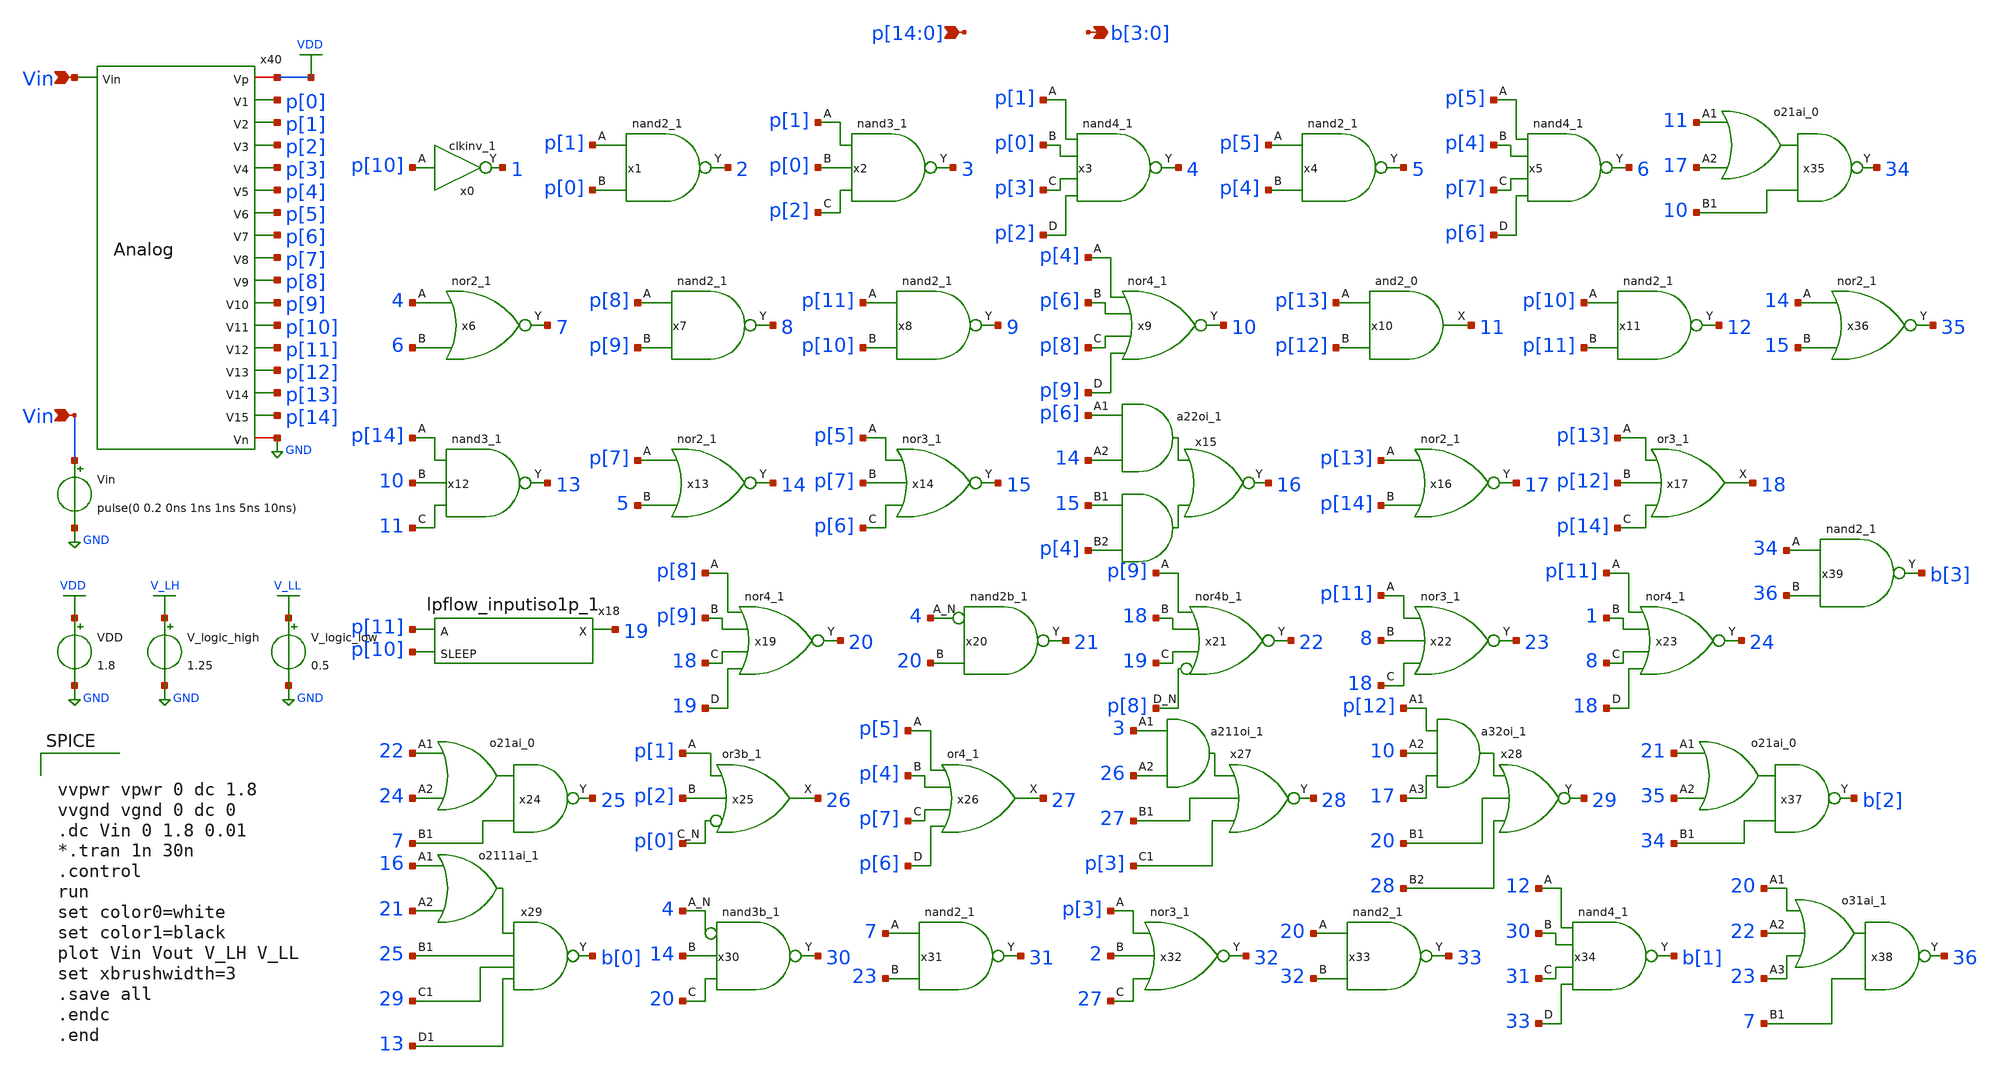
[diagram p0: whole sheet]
** sch_path: xschem/Vth_sch/Pre_layout/analog_therm.sch
**.subckt analog_therm
*+ p[14],p[13],p[12],p[11],p[10],p[9],p[8],p[7],p[6],p[5],p[4],p[3],p[2],p[1],p[0] b[3],b[2],b[1],b[0] Vin Vin
*.ipin p[14],p[13],p[12],p[11],p[10],p[9],p[8],p[7],p[6],p[5],p[4],p[3],p[2],p[1],p[0]
*.opin b[3],b[2],b[1],b[0]
*.ipin Vin
*.ipin Vin
x0 p[10] VGND VNB VPB VPWR 1 sky130_fd_sc_hd__clkinv_1
x1 p[1] p[0] VGND VNB VPB VPWR 2 sky130_fd_sc_hd__nand2_1
x2 p[1] p[0] p[2] VGND VNB VPB VPWR 3 sky130_fd_sc_hd__nand3_1
x3 p[1] p[0] p[3] p[2] VGND VNB VPB VPWR 4 sky130_fd_sc_hd__nand4_1
x4 p[5] p[4] VGND VNB VPB VPWR 5 sky130_fd_sc_hd__nand2_1
x5 p[5] p[4] p[7] p[6] VGND VNB VPB VPWR 6 sky130_fd_sc_hd__nand4_1
x6 4 6 VGND VNB VPB VPWR 7 sky130_fd_sc_hd__nor2_1
x7 p[8] p[9] VGND VNB VPB VPWR 8 sky130_fd_sc_hd__nand2_1
x8 p[11] p[10] VGND VNB VPB VPWR 9 sky130_fd_sc_hd__nand2_1
x9 p[4] p[6] p[8] p[9] VGND VNB VPB VPWR 10 sky130_fd_sc_hd__nor4_1
x10 p[13] p[12] VGND VNB VPB VPWR 11 sky130_fd_sc_hd__and2_0
x11 p[10] p[11] VGND VNB VPB VPWR 12 sky130_fd_sc_hd__nand2_1
x12 p[14] 10 11 VGND VNB VPB VPWR 13 sky130_fd_sc_hd__nand3_1
x13 p[7] 5 VGND VNB VPB VPWR 14 sky130_fd_sc_hd__nor2_1
x14 p[5] p[7] p[6] VGND VNB VPB VPWR 15 sky130_fd_sc_hd__nor3_1
x15 p[6] 14 15 p[4] VGND VNB VPB VPWR 16 sky130_fd_sc_hd__a22oi_1
x16 p[13] p[14] VGND VNB VPB VPWR 17 sky130_fd_sc_hd__nor2_1
x17 p[13] p[12] p[14] VGND VNB VPB VPWR 18 sky130_fd_sc_hd__or3_1
x18 p[11] p[10] VGND VNB VPB VPWR 19 sky130_fd_sc_hd__lpflow_inputiso1p_1
x19 p[8] p[9] 18 19 VGND VNB VPB VPWR 20 sky130_fd_sc_hd__nor4_1
x20 4 20 VGND VNB VPB VPWR 21 sky130_fd_sc_hd__nand2b_1
x21 p[9] 18 19 p[8] VGND VNB VPB VPWR 22 sky130_fd_sc_hd__nor4b_1
x22 p[11] 8 18 VGND VNB VPB VPWR 23 sky130_fd_sc_hd__nor3_1
x23 p[11] 1 8 18 VGND VNB VPB VPWR 24 sky130_fd_sc_hd__nor4_1
x24 22 24 7 VGND VNB VPB VPWR 25 sky130_fd_sc_hd__o21ai_0
x25 p[1] p[2] p[0] VGND VNB VPB VPWR 26 sky130_fd_sc_hd__or3b_1
x26 p[5] p[4] p[7] p[6] VGND VNB VPB VPWR 27 sky130_fd_sc_hd__or4_1
x27 3 26 27 p[3] VGND VNB VPB VPWR 28 sky130_fd_sc_hd__a211oi_1
x28 p[12] 10 17 20 28 VGND VNB VPB VPWR 29 sky130_fd_sc_hd__a32oi_1
x29 16 21 25 29 13 VGND VNB VPB VPWR b[0] sky130_fd_sc_hd__o2111ai_1
x30 4 14 20 VGND VNB VPB VPWR 30 sky130_fd_sc_hd__nand3b_1
x31 7 23 VGND VNB VPB VPWR 31 sky130_fd_sc_hd__nand2_1
x32 p[3] 2 27 VGND VNB VPB VPWR 32 sky130_fd_sc_hd__nor3_1
x33 20 32 VGND VNB VPB VPWR 33 sky130_fd_sc_hd__nand2_1
x34 12 30 31 33 VGND VNB VPB VPWR b[1] sky130_fd_sc_hd__nand4_1
x35 11 17 10 VGND VNB VPB VPWR 34 sky130_fd_sc_hd__o21ai_0
x36 14 15 VGND VNB VPB VPWR 35 sky130_fd_sc_hd__nor2_1
x37 21 35 34 VGND VNB VPB VPWR b[2] sky130_fd_sc_hd__o21ai_0
x38 20 22 23 7 VGND VNB VPB VPWR 36 sky130_fd_sc_hd__o31ai_1
x39 34 36 VGND VNB VPB VPWR b[3] sky130_fd_sc_hd__nand2_1
x40 VDD Vin p[0] p[1] p[2] p[3] p[4] p[5] p[6] p[7] p[8] p[9] p[10] p[11] p[12] p[13] p[14] GND
+ Analog
V_logic_high V_LH GND 1.25
V_logic_low V_LL GND 0.5
VDD VDD GND 1.8
Vin Vin GND pulse(0 0.2 0ns 1ns 1ns 5ns 10ns)
**** begin user architecture code


vvpwr vpwr 0 dc 1.8
vvgnd vgnd 0 dc 0
.dc Vin 0 1.8 0.01
*.tran 1n 30n
.control
run
set color0=white
set color1=black
plot Vin Vout V_LH V_LL
set xbrushwidth=3
.save all
.endc
.end


 .lib $::SKYWATER_MODELS/sky130.lib.spice tt
.include $::SKYWATER_STDCELLS/sky130_fd_sc_hd.spice

**** end user architecture code
**.ends
.GLOBAL V_LH
.GLOBAL GND
.GLOBAL V_LL
.GLOBAL VDD
.end
